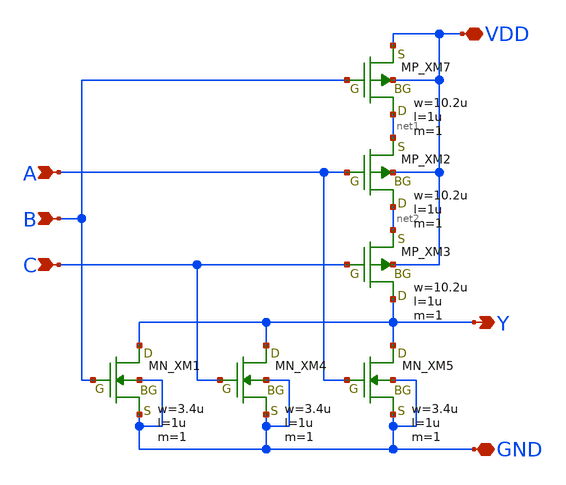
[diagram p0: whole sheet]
** sch_path: openIP62_rev1.0/IP62/Technology/tech/symbols/Xschem/IP62_5_stdcell/NOR3.sch
**.subckt NOR3 A B Y VDD GND C
*.ipin A
*.ipin B
*.opin Y
*.iopin VDD
*.iopin GND
*.ipin C
XM7 net1 B VDD VDD PMOS w=10.2u l=1u as=0 ad=0 ps=0 pd=0 nrd=0 nrs=0 m=1
XM2 net2 A net1 VDD PMOS w=10.2u l=1u as=0 ad=0 ps=0 pd=0 nrd=0 nrs=0 m=1
XM3 Y C net2 VDD PMOS w=10.2u l=1u as=0 ad=0 ps=0 pd=0 nrd=0 nrs=0 m=1
XM1 Y B GND GND NMOS w=3.4u l=1u as=0 ad=0 ps=0 pd=0 nrd=0 nrs=0 m=1
XM4 Y C GND GND NMOS w=3.4u l=1u as=0 ad=0 ps=0 pd=0 nrd=0 nrs=0 m=1
XM5 Y A GND GND NMOS w=3.4u l=1u as=0 ad=0 ps=0 pd=0 nrd=0 nrs=0 m=1
**.ends
.end
